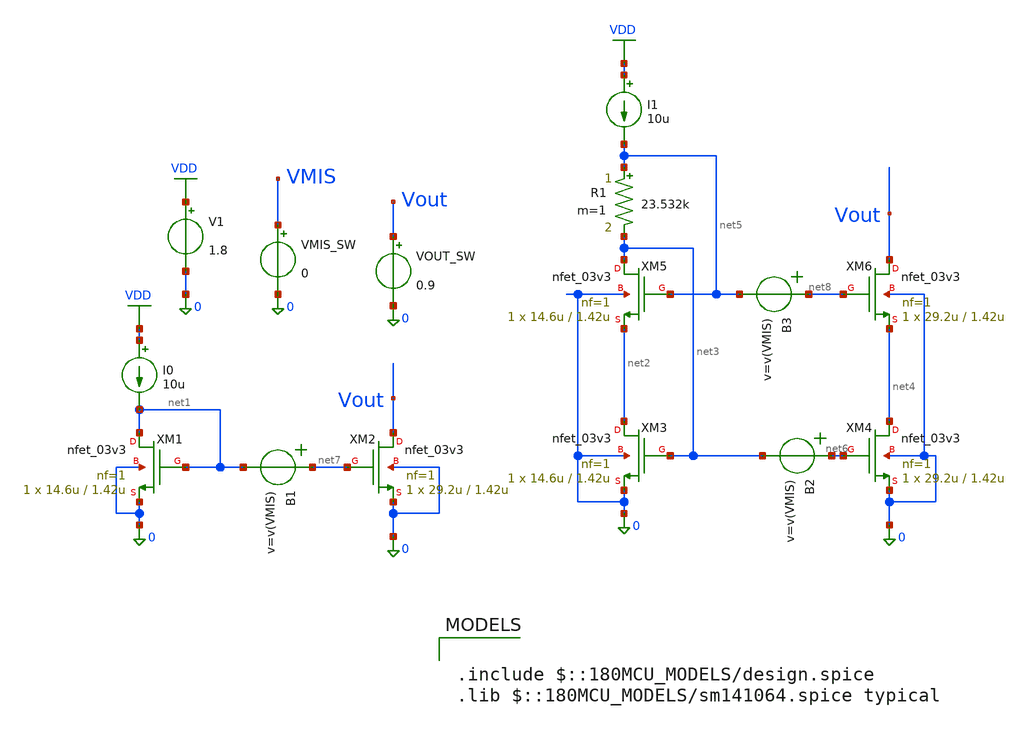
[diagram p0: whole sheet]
** sch_path: Lab_05/CMirror.sch
**.subckt CMirror
I0 VDD net1 10u
XM1 net1 net1 0 0 nfet_03v3 L=1.42u W=14.6u nf=1 ad='int((nf+1)/2) * W/nf * 0.18u' as='int((nf+2)/2) * W/nf * 0.18u'
+ pd='2*int((nf+1)/2) * (W/nf + 0.18u)' ps='2*int((nf+2)/2) * (W/nf + 0.18u)' nrd='0.18u / W' nrs='0.18u / W'
+ sa=0 sb=0 sd=0 m=1
XM2 Vout net7 0 0 nfet_03v3 L=1.42u W=29.2u nf=1 ad='int((nf+1)/2) * W/nf * 0.18u' as='int((nf+2)/2) * W/nf * 0.18u'
+ pd='2*int((nf+1)/2) * (W/nf + 0.18u)' ps='2*int((nf+2)/2) * (W/nf + 0.18u)' nrd='0.18u / W' nrs='0.18u / W'
+ sa=0 sb=0 sd=0 m=1
V1 VDD 0 1.8
XM3 net2 net3 0 0 nfet_03v3 L=1.42u W=14.6u nf=1 ad='int((nf+1)/2) * W/nf * 0.18u' as='int((nf+2)/2) * W/nf * 0.18u'
+ pd='2*int((nf+1)/2) * (W/nf + 0.18u)' ps='2*int((nf+2)/2) * (W/nf + 0.18u)' nrd='0.18u / W' nrs='0.18u / W'
+ sa=0 sb=0 sd=0 m=1
XM4 net4 net6 0 0 nfet_03v3 L=1.42u W=29.2u nf=1 ad='int((nf+1)/2) * W/nf * 0.18u' as='int((nf+2)/2) * W/nf * 0.18u'
+ pd='2*int((nf+1)/2) * (W/nf + 0.18u)' ps='2*int((nf+2)/2) * (W/nf + 0.18u)' nrd='0.18u / W' nrs='0.18u / W'
+ sa=0 sb=0 sd=0 m=1
XM5 net3 net5 net2 0 nfet_03v3 L=1.42u W=14.6u nf=1 ad='int((nf+1)/2) * W/nf * 0.18u' as='int((nf+2)/2) * W/nf * 0.18u'
+ pd='2*int((nf+1)/2) * (W/nf + 0.18u)' ps='2*int((nf+2)/2) * (W/nf + 0.18u)' nrd='0.18u / W' nrs='0.18u / W'
+ sa=0 sb=0 sd=0 m=1
I1 VDD net5 10u
R1 net5 net3 23.532k m=1
XM6 Vout net8 net4 0 nfet_03v3 L=1.42u W=29.2u nf=1 ad='int((nf+1)/2) * W/nf * 0.18u' as='int((nf+2)/2) * W/nf * 0.18u'
+ pd='2*int((nf+1)/2) * (W/nf + 0.18u)' ps='2*int((nf+2)/2) * (W/nf + 0.18u)' nrd='0.18u / W' nrs='0.18u / W'
+ sa=0 sb=0 sd=0 m=1
B1 net7 net1 v=v(VMIS)
VMIS_SW VMIS 0 0
VOUT_SW Vout 0 0.9
B2 net6 net3 v=v(VMIS)
B3 net8 net5 v=v(VMIS)
**** begin user architecture code

.include $::180MCU_MODELS/design.spice
.lib $::180MCU_MODELS/sm141064.spice typical


.control
alterparam sw_stat_global = 0
alterparam sw_stat_mismatch = 0
reset
save all
let x = 1
set num = {$&x}
dowhile x <= 6
save @m.xm{$num}.m0[id]
save @m.xm{$num}.m0[vgs]
save @m.xm{$num}.m0[vds]
save @m.xm{$num}.m0[vdsat]
save @m.xm{$num}.m0[vth]
save @m.xm{$num}.m0[gm]
save @m.xm{$num}.m0[gds]
save @m.xm{$num}.m0[gmbs]
save @m.xm{$num}.m0[cgg]
save @m.xm{$num}.m0[cdd]
save @m.xm{$num}.m0[css]
let x = x + 1
set num = {$&x}
end
save all
* tighten the tolerances to improve the accuracy
*option reltol=1e-5 vntol=1e-6 abstol=1e-12
dc VOUT_SW 0 1.8 10m
echo "Simple Current Mirror Simulation Results"
meas dc i1 find @m.xm2.m0[id] when v(VOUT)=0.5V
meas dc i2 find @m.xm2.m0[id] when v(VOUT)=1.5V
let perc_change = (i2 - i1) / ((i2 + i1)/2) * 100
print perc_change
echo "Wide Swing Current Mirror Simulation Results"
meas dc i1 find @m.xm4.m0[id] when v(VOUT)=0.5V
meas dc i2 find @m.xm4.m0[id] when v(VOUT)=1.5V
let perc_change = (i2 - i1) / ((i2 + i1)/2) * 100

print perc_change
* Rout calculation
let Rout1 = 1/deriv(@m.xm2.m0[id])
let Rout2 = 1/deriv(@m.xm4.m0[id])
* Percent error calculation
let Error1 = (@m.xm2.m0[id] - 20u) / 20u * 100
let Error2 = (@m.xm4.m0[id] - 20u) / 20u * 100
write cmirror_dc.raw
.endc

**** end user architecture code
**.ends
.GLOBAL VDD
.end
